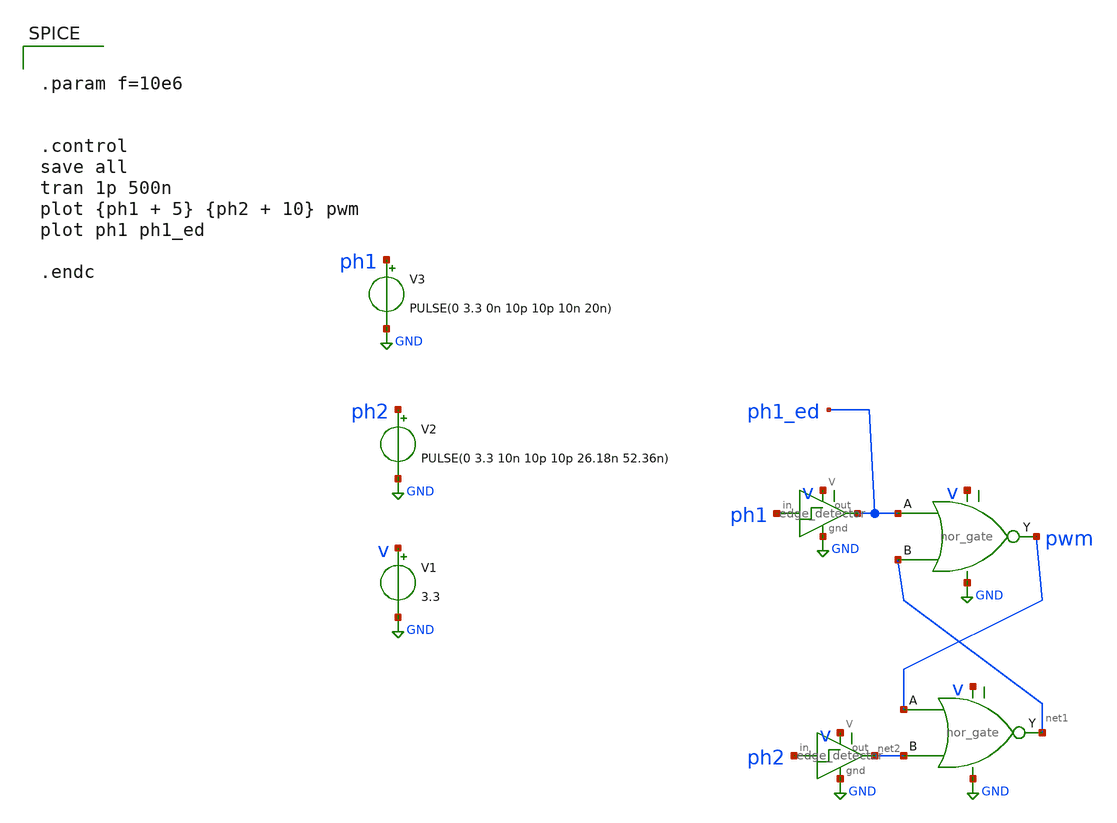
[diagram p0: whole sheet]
** sch_path: xschem/tb_pd.sch
**.subckt tb_pd
V1 v GND 3.3
V2 ph2 GND PULSE(0 3.3 10n 10p 10p 26.18n 52.36n)
X3 v GND ph1 ph1_ed edge_detector
X4 pwm net1 ph1_ed v GND nor_gate
X5 net1 net2 pwm v GND nor_gate
X6 v GND ph2 net2 edge_detector
V3 ph1 GND PULSE(0 3.3 0n 10p 10p 10n 20n)
**** begin user architecture code

.include /foss/pdks/gf180mcuC/libs.tech/ngspice/design.ngspice
.lib /foss/pdks/gf180mcuC/libs.tech/ngspice/sm141064.ngspice typical
.lib /foss/pdks/gf180mcuC/libs.tech/ngspice/sm141064.ngspice mimcap_statistical
.lib /foss/pdks/gf180mcuC/libs.tech/ngspice/sm141064.ngspice cap_mim



.param f=10e6


.control
save all
tran 1p 500n
plot {ph1 + 5} {ph2 + 10} pwm
plot ph1 ph1_ed

.endc

**** end user architecture code
**.ends
.GLOBAL GND
.end
